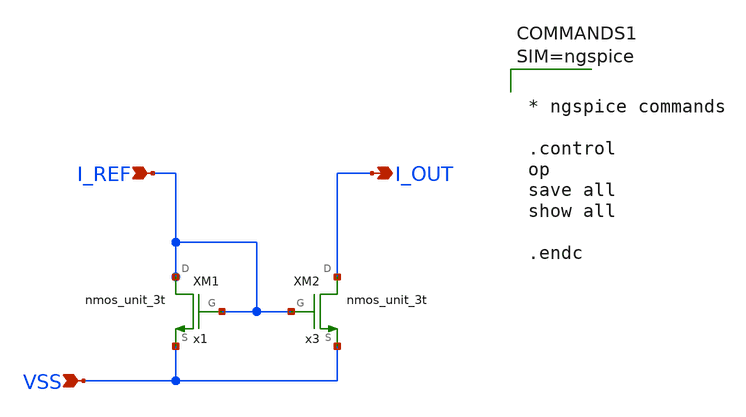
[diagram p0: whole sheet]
** sch_path: designs/analog_library/bias_1.sch
**.subckt bias_1 I_REF I_OUT VSS
*.ipin I_REF
*.opin I_OUT
*.ipin VSS
XM2 I_OUT I_REF VSS nmos_unit_3t M=3
XM1 I_REF I_REF VSS nmos_unit_3t M=1
**** begin user architecture code



* ngspice commands

.control
op
save all
show all

.endc





** opencircuitdesign pdks install
.lib $::SKYWATER_MODELS/sky130.lib.spice tt




* stimulus
V1 VSS GND 0
I0 GND I_REF 50u
V2 I_OUT GND 1


**** end user architecture code
**.ends

* expanding   symbol:  /foss/designs/analog_library/sym/nmos_unit_3t.sym # of pins=3
** sym_path: designs/analog_library/sym/nmos_unit_3t.sym
** sch_path: designs/analog_library/sym/nmos_unit_3t.sch
.subckt nmos_unit_3t D G S
*.ipin G
*.iopin S
*.iopin D
XM1 D G S VSS sky130_fd_pr__nfet_01v8 L=0.15 W=2 nf=2 ad='int((nf+1)/2) * W/nf * 0.29' as='int((nf+2)/2) * W/nf * 0.29'
+ pd='2*int((nf+1)/2) * (W/nf + 0.29)' ps='2*int((nf+2)/2) * (W/nf + 0.29)' nrd='0.29 / W' nrs='0.29 / W'
+ sa=0 sb=0 sd=0 mult=1 m=1
**** begin user architecture code
.param M
**** end user architecture code
.ends

.end
